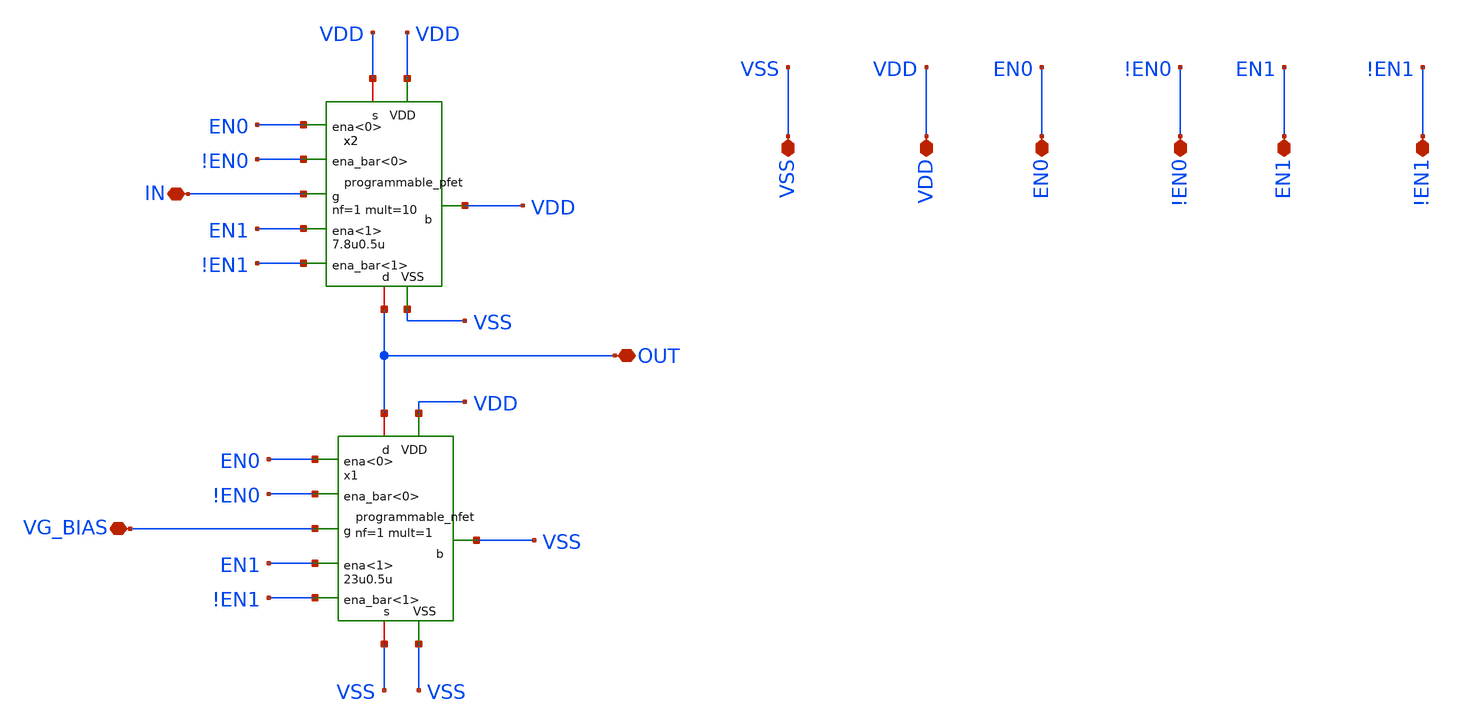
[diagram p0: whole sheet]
** sch_path: designs/libs/core_amps/cs_stage/prgrm_schem/programmable_common_source.sch
**.subckt programmable_common_source VSS VDD EN0 !EN0 EN1 !EN1 OUT IN VG_BIAS
*.iopin VSS
*.iopin VDD
*.iopin EN0
*.iopin !EN0
*.iopin EN1
*.iopin !EN1
*.iopin OUT
*.iopin IN
*.iopin VG_BIAS
x1 OUT VSS VG_BIAS VSS !EN0 VDD !EN1 EN0 EN1 VSS programmable_nfet width=23u length=0.5u nf=1 mult=1
x2 OUT VDD IN VDD !EN0 VDD !EN1 EN0 EN1 VSS programmable_pfet width=7.8u length=0.5u nf=1 mult=10
**.ends

* expanding   symbol:  libs/core_digital/schem/programmable_nfet.sym # of pins=10
** sym_path: designs/libs/core_digital/schem/programmable_nfet.sym
** sch_path: designs/libs/core_digital/schem/programmable_nfet.sch
.subckt programmable_nfet d b g s ena_bar<0> VDD ena_bar<1> ena<0> ena<1> VSS  width=0.22u
+ length=0.28u nf=1 mult=1
*.ipin VSS
*.ipin VDD
*.ipin g
*.ipin ena_bar<1>
*.ipin ena_bar<0>
*.ipin ena<1>
*.ipin ena<0>
*.iopin d
*.iopin s
*.ipin b
XM1 d net2 s b nfet_03v3 L={length} W={width} nf={nf} ad='int((nf+1)/2) * W/nf * 0.18u' as='int((nf+2)/2) * W/nf * 0.18u'
+ pd='2*int((nf+1)/2) * (W/nf + 0.18u)' ps='2*int((nf+2)/2) * (W/nf + 0.18u)' nrd='0.18u / W' nrs='0.18u / W'
+ sa=0 sb=0 sd=0 m={mult}
XM3 d net1 s b nfet_03v3 L={length} W={2*width} nf={2*nf} ad='int((nf+1)/2) * W/nf * 0.18u' as='int((nf+2)/2) * W/nf * 0.18u'
+ pd='2*int((nf+1)/2) * (W/nf + 0.18u)' ps='2*int((nf+2)/2) * (W/nf + 0.18u)' nrd='0.18u / W' nrs='0.18u / W'
+ sa=0 sb=0 sd=0 m={mult}
XM2 net1 ena_bar<1> VSS VSS nfet_03v3 L=0.28u W=0.22u nf=1 ad='int((nf+1)/2) * W/nf * 0.18u' as='int((nf+2)/2) * W/nf * 0.18u'
+ pd='2*int((nf+1)/2) * (W/nf + 0.18u)' ps='2*int((nf+2)/2) * (W/nf + 0.18u)' nrd='0.18u / W' nrs='0.18u / W'
+ sa=0 sb=0 sd=0 m=1
XM4 net2 ena_bar<0> VSS VSS nfet_03v3 L=0.28u W=0.22u nf=1 ad='int((nf+1)/2) * W/nf * 0.18u' as='int((nf+2)/2) * W/nf * 0.18u'
+ pd='2*int((nf+1)/2) * (W/nf + 0.18u)' ps='2*int((nf+2)/2) * (W/nf + 0.18u)' nrd='0.18u / W' nrs='0.18u / W'
+ sa=0 sb=0 sd=0 m=1
x1 ena_bar<0> VDD net2 g VSS ena<0> transmission_gate
x2 ena_bar<1> VDD net1 g VSS ena<1> transmission_gate
.ends


* expanding   symbol:  libs/core_digital/schem/programmable_pfet.sym # of pins=10
** sym_path: designs/libs/core_digital/schem/programmable_pfet.sym
** sch_path: designs/libs/core_digital/schem/programmable_pfet.sch
.subckt programmable_pfet d b g s ena_bar<0> VDD ena_bar<1> ena<0> ena<1> VSS  width=0.22u
+ length=0.28u nf=1 mult=1
*.ipin VSS
*.ipin VDD
*.ipin g
*.ipin ena_bar<1>
*.ipin ena_bar<0>
*.ipin ena<0>
*.iopin s
*.iopin d
*.ipin b
*.ipin ena<1>
XM1 d net2 s b pfet_03v3 L={length} W={width} nf={nf} ad='int((nf+1)/2) * W/nf * 0.18u' as='int((nf+2)/2) * W/nf * 0.18u'
+ pd='2*int((nf+1)/2) * (W/nf + 0.18u)' ps='2*int((nf+2)/2) * (W/nf + 0.18u)' nrd='0.18u / W' nrs='0.18u / W'
+ sa=0 sb=0 sd=0 m={mult}
XM3 d net1 s b pfet_03v3 L={length} W={2*width} nf={2*nf} ad='int((nf+1)/2) * W/nf * 0.18u' as='int((nf+2)/2) * W/nf * 0.18u'
+ pd='2*int((nf+1)/2) * (W/nf + 0.18u)' ps='2*int((nf+2)/2) * (W/nf + 0.18u)' nrd='0.18u / W' nrs='0.18u / W'
+ sa=0 sb=0 sd=0 m={mult}
XM2 net1 ena<1> VDD VDD pfet_03v3 L=0.28u W=0.22u nf=1 ad='int((nf+1)/2) * W/nf * 0.18u' as='int((nf+2)/2) * W/nf * 0.18u'
+ pd='2*int((nf+1)/2) * (W/nf + 0.18u)' ps='2*int((nf+2)/2) * (W/nf + 0.18u)' nrd='0.18u / W' nrs='0.18u / W'
+ sa=0 sb=0 sd=0 m=1
XM4 net2 ena<0> VDD VDD pfet_03v3 L=0.28u W=0.22u nf=1 ad='int((nf+1)/2) * W/nf * 0.18u' as='int((nf+2)/2) * W/nf * 0.18u'
+ pd='2*int((nf+1)/2) * (W/nf + 0.18u)' ps='2*int((nf+2)/2) * (W/nf + 0.18u)' nrd='0.18u / W' nrs='0.18u / W'
+ sa=0 sb=0 sd=0 m=1
x1 ena_bar<0> VDD net2 g VSS ena<0> transmission_gate
x2 ena_bar<1> VDD net1 g VSS ena<1> transmission_gate
.ends


* expanding   symbol:  libs/core_digital/schem/transmission_gate.sym # of pins=6
** sym_path: designs/libs/core_digital/schem/transmission_gate.sym
** sch_path: designs/libs/core_digital/schem/transmission_gate.sch
.subckt transmission_gate ena_bar VDD out in VSS ena
*.ipin in
*.ipin ena_bar
*.ipin ena
*.ipin VSS
*.ipin VDD
*.opin out
XM1 in ena_bar out VDD pfet_03v3 L=0.28u W=0.22u nf=1 ad='int((nf+1)/2) * W/nf * 0.18u' as='int((nf+2)/2) * W/nf * 0.18u'
+ pd='2*int((nf+1)/2) * (W/nf + 0.18u)' ps='2*int((nf+2)/2) * (W/nf + 0.18u)' nrd='0.18u / W' nrs='0.18u / W'
+ sa=0 sb=0 sd=0 m=1
XM2 in ena out VSS nfet_03v3 L=0.28u W=0.22u nf=1 ad='int((nf+1)/2) * W/nf * 0.18u' as='int((nf+2)/2) * W/nf * 0.18u'
+ pd='2*int((nf+1)/2) * (W/nf + 0.18u)' ps='2*int((nf+2)/2) * (W/nf + 0.18u)' nrd='0.18u / W' nrs='0.18u / W'
+ sa=0 sb=0 sd=0 m=1
.ends

.end
